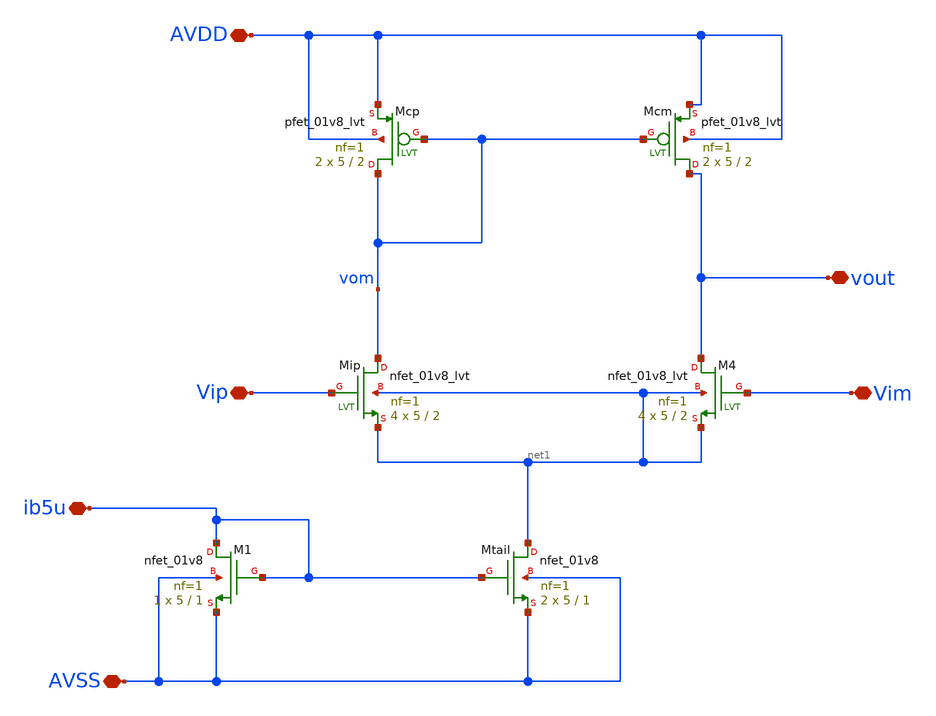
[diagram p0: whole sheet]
** sch_path: xschem/opam.sch
**.subckt opam AVSS ib5u AVDD Vip vout Vim
*.iopin AVSS
*.iopin ib5u
*.iopin AVDD
*.iopin Vip
*.iopin vout
*.iopin Vim
XMtail net1 ib5u AVSS AVSS sky130_fd_pr__nfet_01v8 L=1 W=5 nf=1 ad='int((1 + 1)/2) * 5 / 1 * 0.29' as='int((1 + 2)/2) * 5 / 1 * 0.29'
+ pd='2*int((1 + 1)/2) * (5 / 1 + 0.29)' ps='2*int((1 + 2)/2) * (5 / 1 + 0.29)' nrd='0.29 / 5 ' nrs='0.29 / 5 '
+ sa=0 sb=0 sd=0 mult=2 m=2
XM1 ib5u ib5u AVSS AVSS sky130_fd_pr__nfet_01v8 L=1 W=5 nf=1 ad='int((1 + 1)/2) * 5 / 1 * 0.29' as='int((1 + 2)/2) * 5 / 1 * 0.29'
+ pd='2*int((1 + 1)/2) * (5 / 1 + 0.29)' ps='2*int((1 + 2)/2) * (5 / 1 + 0.29)' nrd='0.29 / 5 ' nrs='0.29 / 5 '
+ sa=0 sb=0 sd=0 mult=1 m=1
XMip vom Vip net1 net1 sky130_fd_pr__nfet_01v8_lvt L=2 W=5 nf=1 ad='int((1 + 1)/2) * 5 / 1 * 0.29' as='int((1 + 2)/2) * 5 / 1 * 0.29'
+ pd='2*int((1 + 1)/2) * (5 / 1 + 0.29)' ps='2*int((1 + 2)/2) * (5 / 1 + 0.29)' nrd='0.29 / 5 ' nrs='0.29 / 5 '
+ sa=0 sb=0 sd=0 mult=4 m=4
XM4 vout Vim net1 net1 sky130_fd_pr__nfet_01v8_lvt L=2 W=5 nf=1 ad='int((1 + 1)/2) * 5 / 1 * 0.29' as='int((1 + 2)/2) * 5 / 1 * 0.29'
+ pd='2*int((1 + 1)/2) * (5 / 1 + 0.29)' ps='2*int((1 + 2)/2) * (5 / 1 + 0.29)' nrd='0.29 / 5 ' nrs='0.29 / 5 '
+ sa=0 sb=0 sd=0 mult=4 m=4
XMcp vom vom AVDD AVDD sky130_fd_pr__pfet_01v8_lvt L=2 W=5 nf=1 ad='int((1 + 1)/2) * 5 / 1 * 0.29' as='int((1 + 2)/2) * 5 / 1 * 0.29'
+ pd='2*int((1 + 1)/2) * (5 / 1 + 0.29)' ps='2*int((1 + 2)/2) * (5 / 1 + 0.29)' nrd='0.29 / 5 ' nrs='0.29 / 5 '
+ sa=0 sb=0 sd=0 mult=2 m=2
XMcm vout vom AVDD AVDD sky130_fd_pr__pfet_01v8_lvt L=2 W=5 nf=1 ad='int((1 + 1)/2) * 5 / 1 * 0.29' as='int((1 + 2)/2) * 5 / 1 * 0.29'
+ pd='2*int((1 + 1)/2) * (5 / 1 + 0.29)' ps='2*int((1 + 2)/2) * (5 / 1 + 0.29)' nrd='0.29 / 5 ' nrs='0.29 / 5 '
+ sa=0 sb=0 sd=0 mult=2 m=2
**** begin user architecture code

** opencircuitdesign pdks install
.lib $::SKYWATER_MODELS/sky130.lib.spice tt

**** end user architecture code
**.ends
.end
